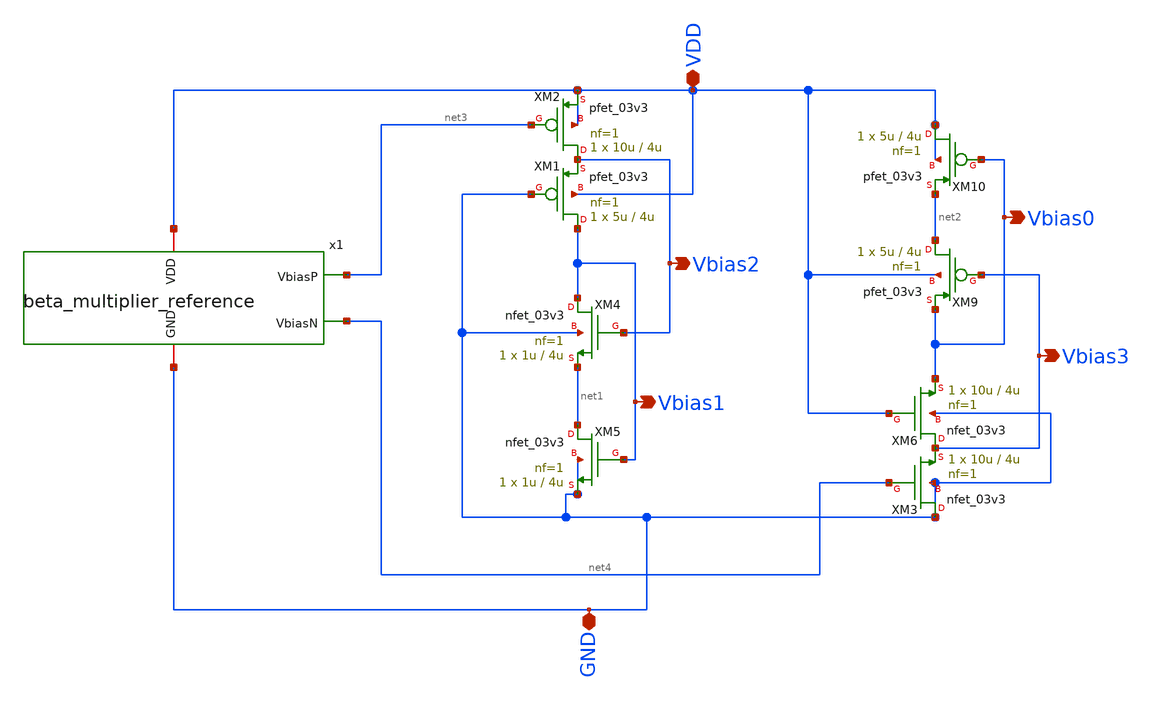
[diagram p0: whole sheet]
** sch_path: analog/OTA_bias.sch
**.subckt OTA_bias VDD Vbias2 Vbias1 Vbias0 Vbias3 GND
*.iopin VDD
*.opin Vbias2
*.opin Vbias1
*.opin Vbias0
*.opin Vbias3
*.iopin GND
XM1 Vbias1 GND Vbias2 VDD pfet_03v3 L=4u W=5u nf=1 ad='int((nf+1)/2) * W/nf * 0.18u' as='int((nf+2)/2) * W/nf * 0.18u'
+ pd='2*int((nf+1)/2) * (W/nf + 0.18u)' ps='2*int((nf+2)/2) * (W/nf + 0.18u)' nrd='0.18u / W' nrs='0.18u / W'
+ sa=0 sb=0 sd=0 m=1
XM4 Vbias1 Vbias2 net1 GND nfet_03v3 L=4u W=1u nf=1 ad='int((nf+1)/2) * W/nf * 0.18u' as='int((nf+2)/2) * W/nf * 0.18u'
+ pd='2*int((nf+1)/2) * (W/nf + 0.18u)' ps='2*int((nf+2)/2) * (W/nf + 0.18u)' nrd='0.18u / W' nrs='0.18u / W'
+ sa=0 sb=0 sd=0 m=1
XM5 net1 Vbias1 GND GND nfet_03v3 L=4u W=1u nf=1 ad='int((nf+1)/2) * W/nf * 0.18u' as='int((nf+2)/2) * W/nf * 0.18u'
+ pd='2*int((nf+1)/2) * (W/nf + 0.18u)' ps='2*int((nf+2)/2) * (W/nf + 0.18u)' nrd='0.18u / W' nrs='0.18u / W'
+ sa=0 sb=0 sd=0 m=1
XM9 net2 Vbias3 Vbias0 VDD pfet_03v3 L=4u W=5u nf=1 ad='int((nf+1)/2) * W/nf * 0.18u' as='int((nf+2)/2) * W/nf * 0.18u'
+ pd='2*int((nf+1)/2) * (W/nf + 0.18u)' ps='2*int((nf+2)/2) * (W/nf + 0.18u)' nrd='0.18u / W' nrs='0.18u / W'
+ sa=0 sb=0 sd=0 m=1
XM10 VDD Vbias0 net2 VDD pfet_03v3 L=4u W=5u nf=1 ad='int((nf+1)/2) * W/nf * 0.18u' as='int((nf+2)/2) * W/nf * 0.18u'
+ pd='2*int((nf+1)/2) * (W/nf + 0.18u)' ps='2*int((nf+2)/2) * (W/nf + 0.18u)' nrd='0.18u / W' nrs='0.18u / W'
+ sa=0 sb=0 sd=0 m=1
XM6 Vbias3 VDD Vbias0 GND nfet_03v3 L=4u W=10u nf=1 ad='int((nf+1)/2) * W/nf * 0.18u' as='int((nf+2)/2) * W/nf * 0.18u'
+ pd='2*int((nf+1)/2) * (W/nf + 0.18u)' ps='2*int((nf+2)/2) * (W/nf + 0.18u)' nrd='0.18u / W' nrs='0.18u / W'
+ sa=0 sb=0 sd=0 m=1
x1 VDD net3 net4 GND beta_multiplier_reference cur_factor={cur_factor}
XM2 Vbias2 net3 VDD VDD pfet_03v3 L=4u W=10u nf=1 ad='int((nf+1)/2) * W/nf * 0.18u' as='int((nf+2)/2) * W/nf * 0.18u'
+ pd='2*int((nf+1)/2) * (W/nf + 0.18u)' ps='2*int((nf+2)/2) * (W/nf + 0.18u)' nrd='0.18u / W' nrs='0.18u / W'
+ sa=0 sb=0 sd=0 m=1
XM3 GND net4 Vbias3 GND nfet_03v3 L=4u W=10u nf=1 ad='int((nf+1)/2) * W/nf * 0.18u' as='int((nf+2)/2) * W/nf * 0.18u'
+ pd='2*int((nf+1)/2) * (W/nf + 0.18u)' ps='2*int((nf+2)/2) * (W/nf + 0.18u)' nrd='0.18u / W' nrs='0.18u / W'
+ sa=0 sb=0 sd=0 m=1
**.ends

* expanding   symbol:
*+  AURA-Event-Driven-Mixed-Signal-ASIC-for-Acoustic-Pattern-Detection/analog/beta_multiplier_reference.sym # of pins=4
** sym_path: analog/beta_multiplier_reference.sym
** sch_path: analog/beta_multiplier_reference.sch
.subckt beta_multiplier_reference VDD VbiasP VbiasN GND  length=410u
*.iopin VDD
*.iopin GND
*.opin VbiasP
*.opin VbiasN
XM2 VbiasN VbiasP VDD VDD pfet_03v3 L=4u W=2u nf=1 ad='int((nf+1)/2) * W/nf * 0.18u' as='int((nf+2)/2) * W/nf * 0.18u'
+ pd='2*int((nf+1)/2) * (W/nf + 0.18u)' ps='2*int((nf+2)/2) * (W/nf + 0.18u)' nrd='0.18u / W' nrs='0.18u / W'
+ sa=0 sb=0 sd=0 m=1
XM3 net2 VbiasP VDD VDD pfet_03v3 L=4u W=2u nf=1 ad='int((nf+1)/2) * W/nf * 0.18u' as='int((nf+2)/2) * W/nf * 0.18u'
+ pd='2*int((nf+1)/2) * (W/nf + 0.18u)' ps='2*int((nf+2)/2) * (W/nf + 0.18u)' nrd='0.18u / W' nrs='0.18u / W'
+ sa=0 sb=0 sd=0 m=1
XM6 VbiasN VbiasN GND GND nfet_03v3 L=4u W=10u nf=1 ad='int((nf+1)/2) * W/nf * 0.18u' as='int((nf+2)/2) * W/nf * 0.18u'
+ pd='2*int((nf+1)/2) * (W/nf + 0.18u)' ps='2*int((nf+2)/2) * (W/nf + 0.18u)' nrd='0.18u / W' nrs='0.18u / W'
+ sa=0 sb=0 sd=0 m=1
XM7 net2 VbiasN net1 GND nfet_03v3 L=4u W=10u nf=1 ad='int((nf+1)/2) * W/nf * 0.18u' as='int((nf+2)/2) * W/nf * 0.18u'
+ pd='2*int((nf+1)/2) * (W/nf + 0.18u)' ps='2*int((nf+2)/2) * (W/nf + 0.18u)' nrd='0.18u / W' nrs='0.18u / W'
+ sa=0 sb=0 sd=0 m=4
x1 VDD VbiasP net2 VbiasN VbiasN GND diff_amp
XM1 net4 net4 VDD VDD pfet_03v3 L=40u W=0.22u nf=1 ad='int((nf+1)/2) * W/nf * 0.18u' as='int((nf+2)/2) * W/nf * 0.18u'
+ pd='2*int((nf+1)/2) * (W/nf + 0.18u)' ps='2*int((nf+2)/2) * (W/nf + 0.18u)' nrd='0.18u / W' nrs='0.18u / W'
+ sa=0 sb=0 sd=0 m=1
XM4 VbiasP net3 VbiasN GND nfet_03v3 L=1u W=1u nf=1 ad='int((nf+1)/2) * W/nf * 0.18u' as='int((nf+2)/2) * W/nf * 0.18u'
+ pd='2*int((nf+1)/2) * (W/nf + 0.18u)' ps='2*int((nf+2)/2) * (W/nf + 0.18u)' nrd='0.18u / W' nrs='0.18u / W'
+ sa=0 sb=0 sd=0 m=1
XM5 net3 VbiasN GND GND nfet_03v3 L=10u W=1u nf=1 ad='int((nf+1)/2) * W/nf * 0.18u' as='int((nf+2)/2) * W/nf * 0.18u'
+ pd='2*int((nf+1)/2) * (W/nf + 0.18u)' ps='2*int((nf+2)/2) * (W/nf + 0.18u)' nrd='0.18u / W' nrs='0.18u / W'
+ sa=0 sb=0 sd=0 m=1
XM8 net5 net5 net4 VDD pfet_03v3 L=40u W=0.22u nf=1 ad='int((nf+1)/2) * W/nf * 0.18u' as='int((nf+2)/2) * W/nf * 0.18u'
+ pd='2*int((nf+1)/2) * (W/nf + 0.18u)' ps='2*int((nf+2)/2) * (W/nf + 0.18u)' nrd='0.18u / W' nrs='0.18u / W'
+ sa=0 sb=0 sd=0 m=1
XM9 net3 net5 net5 VDD pfet_03v3 L=40u W=0.22u nf=1 ad='int((nf+1)/2) * W/nf * 0.18u' as='int((nf+2)/2) * W/nf * 0.18u'
+ pd='2*int((nf+1)/2) * (W/nf + 0.18u)' ps='2*int((nf+2)/2) * (W/nf + 0.18u)' nrd='0.18u / W' nrs='0.18u / W'
+ sa=0 sb=0 sd=0 m=1
XR2 GND net1 GND ppolyf_u_2k r_width=2u r_length={length} m=1
.ends


* expanding   symbol:  AURA/diff_amp.sym # of pins=6
** sym_path: analog/diff_amp.sym
** sch_path: analog/diff_amp.sch
.subckt diff_amp VDD Vo V+ V- Vbias VSS
*.iopin VDD
*.iopin VSS
*.ipin V+
*.ipin V-
*.opin Vo
*.ipin Vbias
XM1 net1 V+ net2 VSS nfet_03v3 L=0.28u W=0.22u nf=1 ad='int((nf+1)/2) * W/nf * 0.18u' as='int((nf+2)/2) * W/nf * 0.18u'
+ pd='2*int((nf+1)/2) * (W/nf + 0.18u)' ps='2*int((nf+2)/2) * (W/nf + 0.18u)' nrd='0.18u / W' nrs='0.18u / W'
+ sa=0 sb=0 sd=0 m=1
XM2 net2 Vbias VSS VSS nfet_03v3 L=0.28u W=0.22u nf=1 ad='int((nf+1)/2) * W/nf * 0.18u' as='int((nf+2)/2) * W/nf * 0.18u'
+ pd='2*int((nf+1)/2) * (W/nf + 0.18u)' ps='2*int((nf+2)/2) * (W/nf + 0.18u)' nrd='0.18u / W' nrs='0.18u / W'
+ sa=0 sb=0 sd=0 m=1
XM3 Vo V- net2 VSS nfet_03v3 L=0.28u W=0.22u nf=1 ad='int((nf+1)/2) * W/nf * 0.18u' as='int((nf+2)/2) * W/nf * 0.18u'
+ pd='2*int((nf+1)/2) * (W/nf + 0.18u)' ps='2*int((nf+2)/2) * (W/nf + 0.18u)' nrd='0.18u / W' nrs='0.18u / W'
+ sa=0 sb=0 sd=0 m=1
XM4 Vo net1 VDD VDD pfet_03v3 L=0.28u W=0.22u nf=1 ad='int((nf+1)/2) * W/nf * 0.18u' as='int((nf+2)/2) * W/nf * 0.18u'
+ pd='2*int((nf+1)/2) * (W/nf + 0.18u)' ps='2*int((nf+2)/2) * (W/nf + 0.18u)' nrd='0.18u / W' nrs='0.18u / W'
+ sa=0 sb=0 sd=0 m=1
XM5 net1 net1 VDD VDD pfet_03v3 L=0.28u W=0.22u nf=1 ad='int((nf+1)/2) * W/nf * 0.18u' as='int((nf+2)/2) * W/nf * 0.18u'
+ pd='2*int((nf+1)/2) * (W/nf + 0.18u)' ps='2*int((nf+2)/2) * (W/nf + 0.18u)' nrd='0.18u / W' nrs='0.18u / W'
+ sa=0 sb=0 sd=0 m=1
.ends

.end
